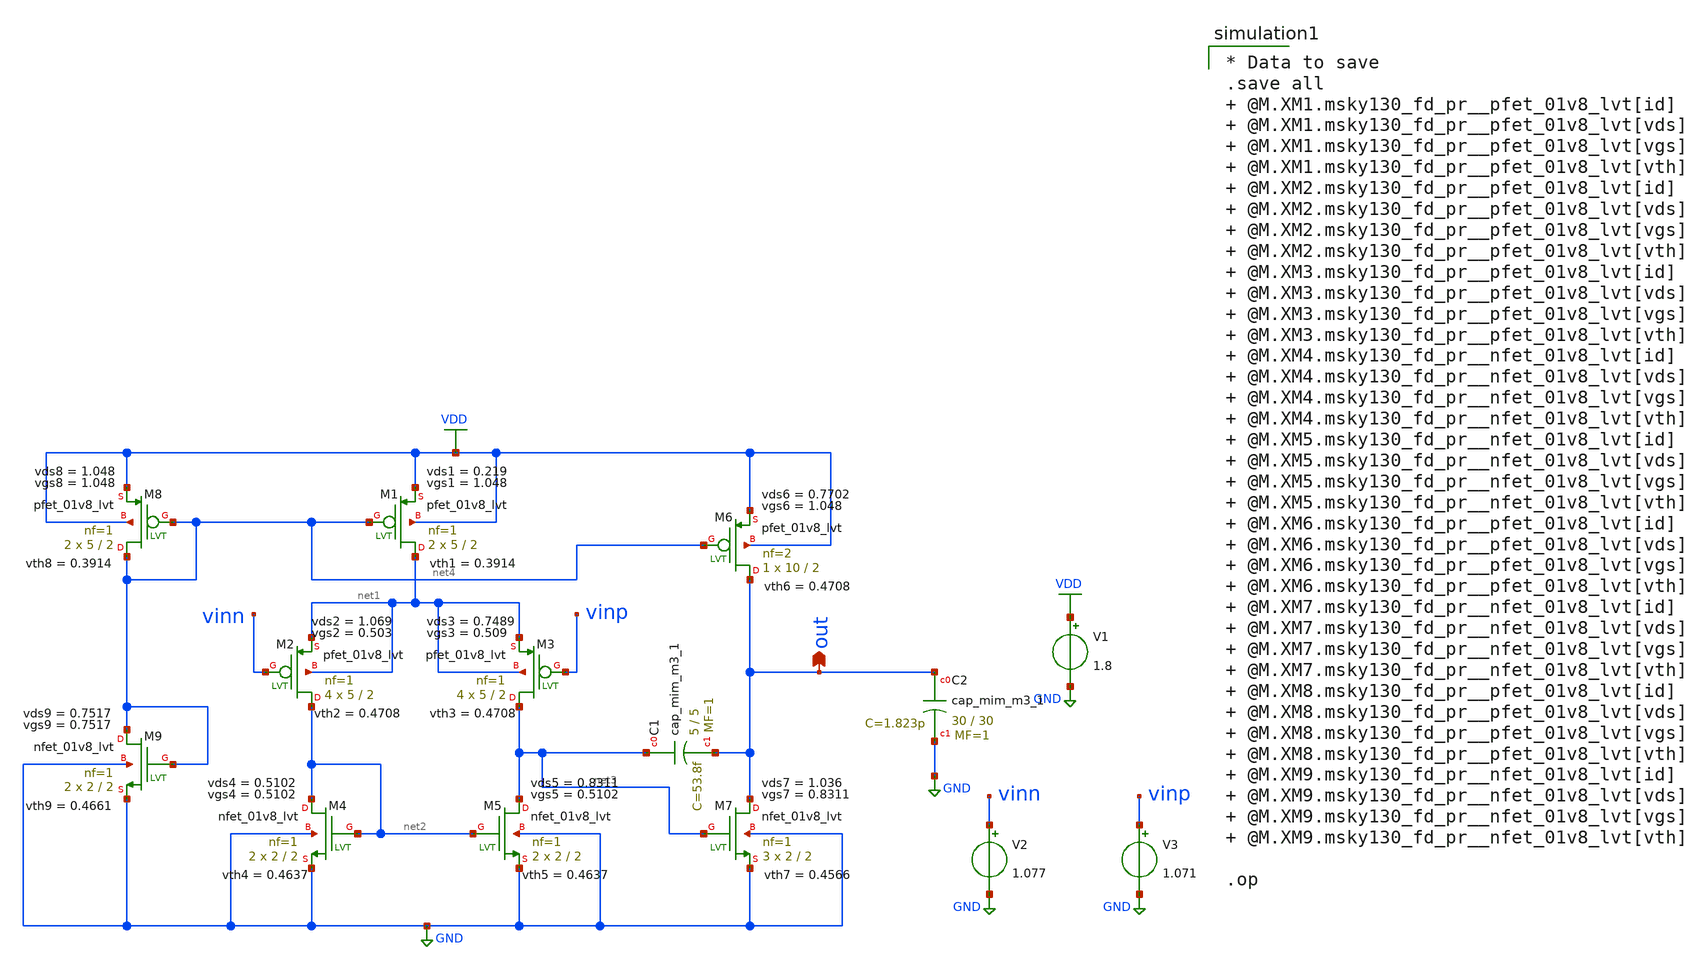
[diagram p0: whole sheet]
** sch_path: OTHER_SOLUTIONS_CONSIDERED/OTHER_BIAS_FOR_TEMPERATURE_SENSOR/OPAMP/XSCHEM/OPAMP_lvt_PMOS_tb_op.sch
**.subckt OPAMP_lvt_PMOS_tb_op out
*.opin out
XC1 net3 out sky130_fd_pr__cap_mim_m3_1 W=5 L=5 MF=1 m=1
XM1 net1 net4 VDD VDD sky130_fd_pr__pfet_01v8_lvt L=2 W=5 nf=1 ad='int((nf+1)/2) * W/nf * 0.29' as='int((nf+2)/2) * W/nf * 0.29'
+ pd='2*int((nf+1)/2) * (W/nf + 0.29)' ps='2*int((nf+2)/2) * (W/nf + 0.29)' nrd='0.29 / W' nrs='0.29 / W'
+ sa=0 sb=0 sd=0 mult=2 m=2
XM2 net2 vinn net1 net1 sky130_fd_pr__pfet_01v8_lvt L=2 W=5 nf=1 ad='int((nf+1)/2) * W/nf * 0.29' as='int((nf+2)/2) * W/nf * 0.29'
+ pd='2*int((nf+1)/2) * (W/nf + 0.29)' ps='2*int((nf+2)/2) * (W/nf + 0.29)' nrd='0.29 / W' nrs='0.29 / W'
+ sa=0 sb=0 sd=0 mult=4 m=4
XM3 net3 vinp net1 net1 sky130_fd_pr__pfet_01v8_lvt L=2 W=5 nf=1 ad='int((nf+1)/2) * W/nf * 0.29' as='int((nf+2)/2) * W/nf * 0.29'
+ pd='2*int((nf+1)/2) * (W/nf + 0.29)' ps='2*int((nf+2)/2) * (W/nf + 0.29)' nrd='0.29 / W' nrs='0.29 / W'
+ sa=0 sb=0 sd=0 mult=4 m=4
XM4 net2 net2 GND GND sky130_fd_pr__nfet_01v8_lvt L=2 W=2 nf=1 ad='int((nf+1)/2) * W/nf * 0.29' as='int((nf+2)/2) * W/nf * 0.29'
+ pd='2*int((nf+1)/2) * (W/nf + 0.29)' ps='2*int((nf+2)/2) * (W/nf + 0.29)' nrd='0.29 / W' nrs='0.29 / W'
+ sa=0 sb=0 sd=0 mult=2 m=2
XM5 net3 net2 GND GND sky130_fd_pr__nfet_01v8_lvt L=2 W=2 nf=1 ad='int((nf+1)/2) * W/nf * 0.29' as='int((nf+2)/2) * W/nf * 0.29'
+ pd='2*int((nf+1)/2) * (W/nf + 0.29)' ps='2*int((nf+2)/2) * (W/nf + 0.29)' nrd='0.29 / W' nrs='0.29 / W'
+ sa=0 sb=0 sd=0 mult=2 m=2
XM6 out net4 VDD VDD sky130_fd_pr__pfet_01v8_lvt L=2 W=10 nf=2 ad='int((nf+1)/2) * W/nf * 0.29' as='int((nf+2)/2) * W/nf * 0.29'
+ pd='2*int((nf+1)/2) * (W/nf + 0.29)' ps='2*int((nf+2)/2) * (W/nf + 0.29)' nrd='0.29 / W' nrs='0.29 / W'
+ sa=0 sb=0 sd=0 mult=1 m=1
XM7 out net3 GND GND sky130_fd_pr__nfet_01v8_lvt L=2 W=2 nf=1 ad='int((nf+1)/2) * W/nf * 0.29' as='int((nf+2)/2) * W/nf * 0.29'
+ pd='2*int((nf+1)/2) * (W/nf + 0.29)' ps='2*int((nf+2)/2) * (W/nf + 0.29)' nrd='0.29 / W' nrs='0.29 / W'
+ sa=0 sb=0 sd=0 mult=3 m=3
XM8 net4 net4 VDD VDD sky130_fd_pr__pfet_01v8_lvt L=2 W=5 nf=1 ad='int((nf+1)/2) * W/nf * 0.29' as='int((nf+2)/2) * W/nf * 0.29'
+ pd='2*int((nf+1)/2) * (W/nf + 0.29)' ps='2*int((nf+2)/2) * (W/nf + 0.29)' nrd='0.29 / W' nrs='0.29 / W'
+ sa=0 sb=0 sd=0 mult=2 m=2
XM9 net4 net4 GND GND sky130_fd_pr__nfet_01v8_lvt L=2 W=2 nf=1 ad='int((nf+1)/2) * W/nf * 0.29' as='int((nf+2)/2) * W/nf * 0.29'
+ pd='2*int((nf+1)/2) * (W/nf + 0.29)' ps='2*int((nf+2)/2) * (W/nf + 0.29)' nrd='0.29 / W' nrs='0.29 / W'
+ sa=0 sb=0 sd=0 mult=2 m=2
V1 VDD GND 1.8
V2 vinn GND 1.077
V3 vinp GND 1.071
XC2 out GND sky130_fd_pr__cap_mim_m3_1 W=30 L=30 MF=1 m=1
**** begin user architecture code

* Data to save
.save all  @M.XM1.msky130_fd_pr__pfet_01v8_lvt[id]  @M.XM1.msky130_fd_pr__pfet_01v8_lvt[vds]  @M.XM1.msky130_fd_pr__pfet_01v8_lvt[vgs]  @M.XM1.msky130_fd_pr__pfet_01v8_lvt[vth]  @M.XM2.msky130_fd_pr__pfet_01v8_lvt[id]  @M.XM2.msky130_fd_pr__pfet_01v8_lvt[vds]  @M.XM2.msky130_fd_pr__pfet_01v8_lvt[vgs]  @M.XM2.msky130_fd_pr__pfet_01v8_lvt[vth]  @M.XM3.msky130_fd_pr__pfet_01v8_lvt[id]  @M.XM3.msky130_fd_pr__pfet_01v8_lvt[vds]  @M.XM3.msky130_fd_pr__pfet_01v8_lvt[vgs]  @M.XM3.msky130_fd_pr__pfet_01v8_lvt[vth]  @M.XM4.msky130_fd_pr__nfet_01v8_lvt[id]  @M.XM4.msky130_fd_pr__nfet_01v8_lvt[vds]  @M.XM4.msky130_fd_pr__nfet_01v8_lvt[vgs]  @M.XM4.msky130_fd_pr__nfet_01v8_lvt[vth]  @M.XM5.msky130_fd_pr__nfet_01v8_lvt[id]  @M.XM5.msky130_fd_pr__nfet_01v8_lvt[vds]  @M.XM5.msky130_fd_pr__nfet_01v8_lvt[vgs]  @M.XM5.msky130_fd_pr__nfet_01v8_lvt[vth]  @M.XM6.msky130_fd_pr__pfet_01v8_lvt[id]  @M.XM6.msky130_fd_pr__pfet_01v8_lvt[vds]  @M.XM6.msky130_fd_pr__pfet_01v8_lvt[vgs]  @M.XM6.msky130_fd_pr__pfet_01v8_lvt[vth]  @M.XM7.msky130_fd_pr__nfet_01v8_lvt[id]  @M.XM7.msky130_fd_pr__nfet_01v8_lvt[vds]  @M.XM7.msky130_fd_pr__nfet_01v8_lvt[vgs]  @M.XM7.msky130_fd_pr__nfet_01v8_lvt[vth]  @M.XM8.msky130_fd_pr__pfet_01v8_lvt[id]  @M.XM8.msky130_fd_pr__pfet_01v8_lvt[vds]  @M.XM8.msky130_fd_pr__pfet_01v8_lvt[vgs]  @M.XM8.msky130_fd_pr__pfet_01v8_lvt[vth]  @M.XM9.msky130_fd_pr__nfet_01v8_lvt[id]  @M.XM9.msky130_fd_pr__nfet_01v8_lvt[vds]  @M.XM9.msky130_fd_pr__nfet_01v8_lvt[vgs]  @M.XM9.msky130_fd_pr__nfet_01v8_lvt[vth]

.op



** opencircuitdesign pdks install
.lib $::SKYWATER_MODELS/sky130.lib.spice tt


**** end user architecture code
**.ends
.GLOBAL VDD
.GLOBAL GND
.end
